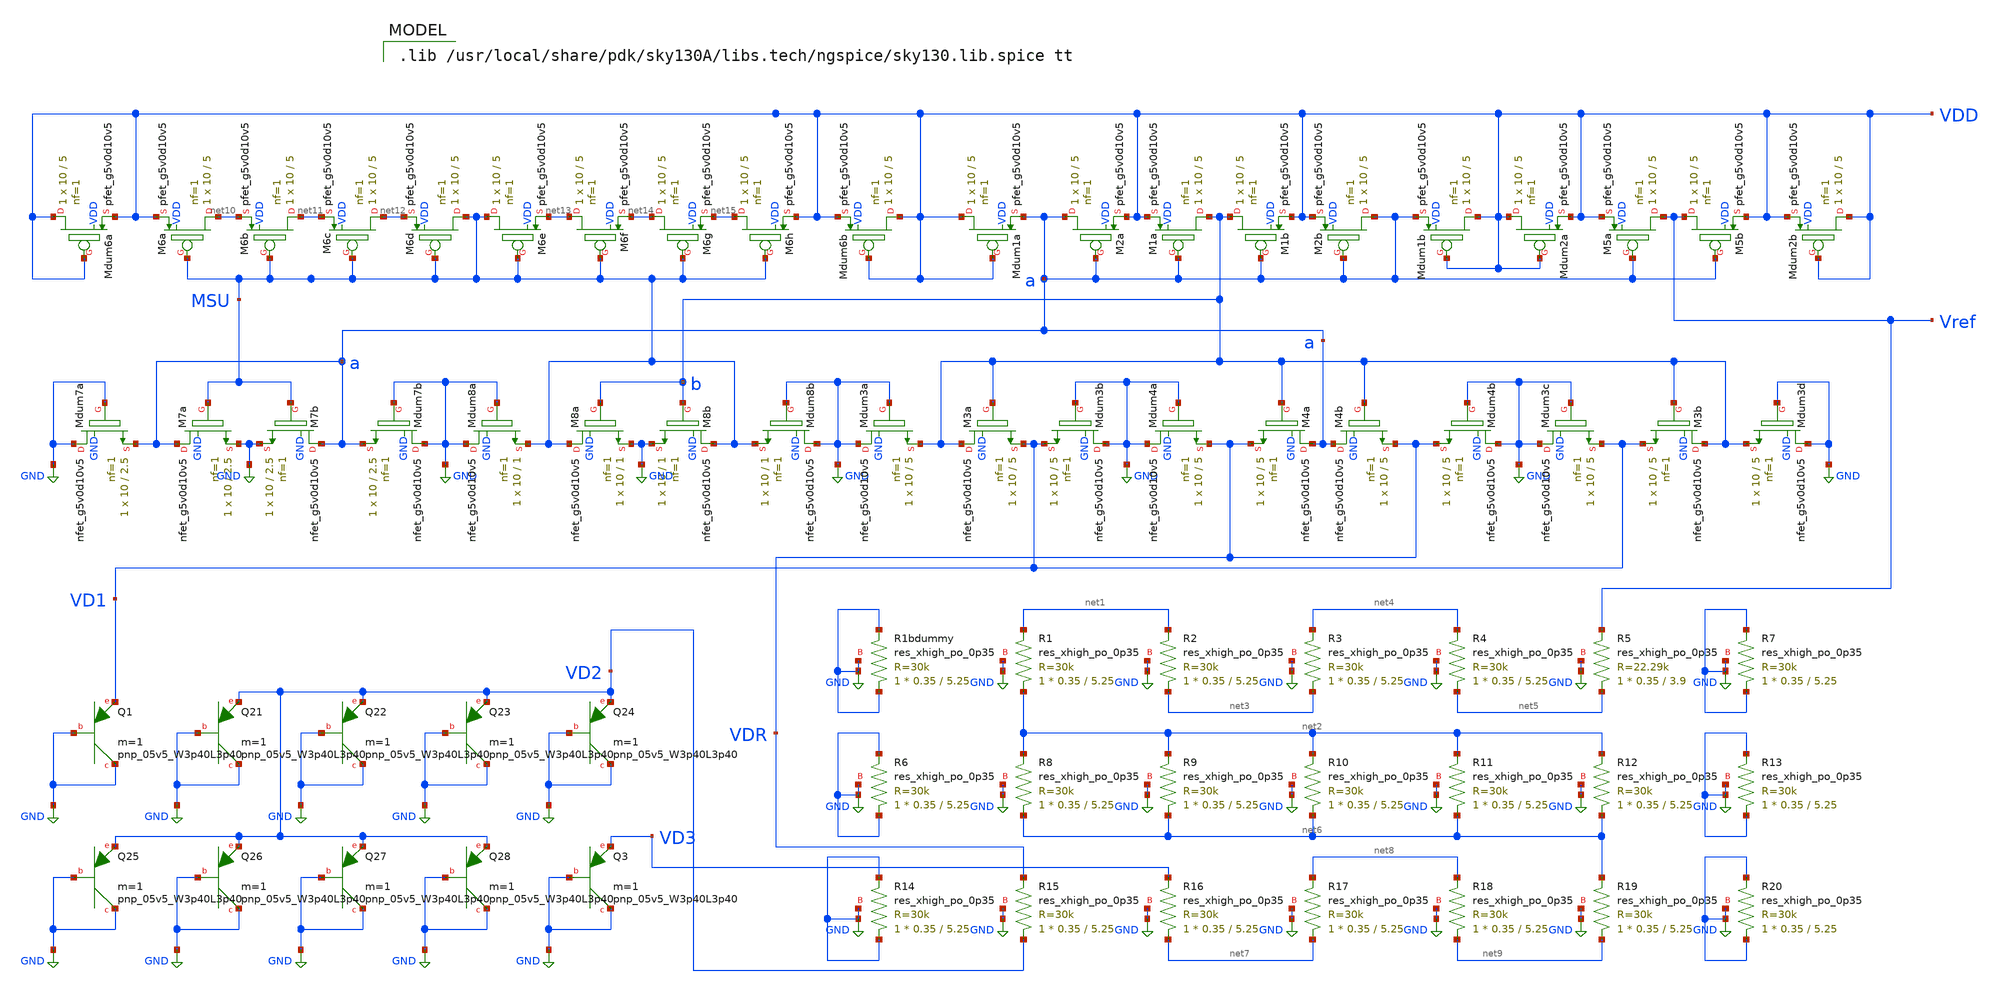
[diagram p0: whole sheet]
** sch_path: 2_BGR_nocas_30k_3p4pnp_floor.sch
**.subckt 2_BGR_nocas_30k_3p4pnp_floor
XM2a a a VDD VDD sky130_fd_pr__pfet_g5v0d10v5 L=5 W=10 nf=1 ad='int((nf+1)/2) * W/nf * 0.29' as='int((nf+2)/2) * W/nf * 0.29'
+ pd='2*int((nf+1)/2) * (W/nf + 0.29)' ps='2*int((nf+2)/2) * (W/nf + 0.29)' nrd='0.29 / W' nrs='0.29 / W'
+ sa=0 sb=0 sd=0 mult=1 m=1
XM1a b a VDD VDD sky130_fd_pr__pfet_g5v0d10v5 L=5 W=10 nf=1 ad='int((nf+1)/2) * W/nf * 0.29' as='int((nf+2)/2) * W/nf * 0.29'
+ pd='2*int((nf+1)/2) * (W/nf + 0.29)' ps='2*int((nf+2)/2) * (W/nf + 0.29)' nrd='0.29 / W' nrs='0.29 / W'
+ sa=0 sb=0 sd=0 mult=1 m=1
XM1b b a VDD VDD sky130_fd_pr__pfet_g5v0d10v5 L=5 W=10 nf=1 ad='int((nf+1)/2) * W/nf * 0.29' as='int((nf+2)/2) * W/nf * 0.29'
+ pd='2*int((nf+1)/2) * (W/nf + 0.29)' ps='2*int((nf+2)/2) * (W/nf + 0.29)' nrd='0.29 / W' nrs='0.29 / W'
+ sa=0 sb=0 sd=0 mult=1 m=1
XM2b a a VDD VDD sky130_fd_pr__pfet_g5v0d10v5 L=5 W=10 nf=1 ad='int((nf+1)/2) * W/nf * 0.29' as='int((nf+2)/2) * W/nf * 0.29'
+ pd='2*int((nf+1)/2) * (W/nf + 0.29)' ps='2*int((nf+2)/2) * (W/nf + 0.29)' nrd='0.29 / W' nrs='0.29 / W'
+ sa=0 sb=0 sd=0 mult=1 m=1
XM5a Vref a VDD VDD sky130_fd_pr__pfet_g5v0d10v5 L=5 W=10 nf=1 ad='int((nf+1)/2) * W/nf * 0.29' as='int((nf+2)/2) * W/nf * 0.29'
+ pd='2*int((nf+1)/2) * (W/nf + 0.29)' ps='2*int((nf+2)/2) * (W/nf + 0.29)' nrd='0.29 / W' nrs='0.29 / W'
+ sa=0 sb=0 sd=0 mult=1 m=1
XM5b Vref a VDD VDD sky130_fd_pr__pfet_g5v0d10v5 L=5 W=10 nf=1 ad='int((nf+1)/2) * W/nf * 0.29' as='int((nf+2)/2) * W/nf * 0.29'
+ pd='2*int((nf+1)/2) * (W/nf + 0.29)' ps='2*int((nf+2)/2) * (W/nf + 0.29)' nrd='0.29 / W' nrs='0.29 / W'
+ sa=0 sb=0 sd=0 mult=1 m=1
XR1bdummy GND GND GND sky130_fd_pr__res_xhigh_po_0p35 L=5.25 mult=1 m=1
XR1 net2 net1 GND sky130_fd_pr__res_xhigh_po_0p35 L=5.25 mult=1 m=1
XR2 net3 net1 GND sky130_fd_pr__res_xhigh_po_0p35 L=5.25 mult=1 m=1
XR3 net3 net4 GND sky130_fd_pr__res_xhigh_po_0p35 L=5.25 mult=1 m=1
XR4 net5 net4 GND sky130_fd_pr__res_xhigh_po_0p35 L=5.25 mult=1 m=1
XR5 net5 Vref GND sky130_fd_pr__res_xhigh_po_0p35 L=3.9 mult=1 m=1
XR8 net6 net2 GND sky130_fd_pr__res_xhigh_po_0p35 L=5.25 mult=1 m=1
XR9 net6 net2 GND sky130_fd_pr__res_xhigh_po_0p35 L=5.25 mult=1 m=1
XR10 net6 net2 GND sky130_fd_pr__res_xhigh_po_0p35 L=5.25 mult=1 m=1
XR11 net6 net2 GND sky130_fd_pr__res_xhigh_po_0p35 L=5.25 mult=1 m=1
XR12 net6 net2 GND sky130_fd_pr__res_xhigh_po_0p35 L=5.25 mult=1 m=1
XR14 GND GND GND sky130_fd_pr__res_xhigh_po_0p35 L=5.25 mult=1 m=1
XR15 VD2 VDR GND sky130_fd_pr__res_xhigh_po_0p35 L=5.25 mult=1 m=1
XR16 net7 VD3 GND sky130_fd_pr__res_xhigh_po_0p35 L=5.25 mult=1 m=1
XR17 net7 net8 GND sky130_fd_pr__res_xhigh_po_0p35 L=5.25 mult=1 m=1
XR18 net9 net8 GND sky130_fd_pr__res_xhigh_po_0p35 L=5.25 mult=1 m=1
XR19 net9 net6 GND sky130_fd_pr__res_xhigh_po_0p35 L=5.25 mult=1 m=1
XQ21 GND GND VD2 sky130_fd_pr__pnp_05v5_W3p40L3p40 m=1
XQ22 GND GND VD2 sky130_fd_pr__pnp_05v5_W3p40L3p40 m=1
XQ23 GND GND VD2 sky130_fd_pr__pnp_05v5_W3p40L3p40 m=1
XQ24 GND GND VD2 sky130_fd_pr__pnp_05v5_W3p40L3p40 m=1
XQ1 GND GND VD1 sky130_fd_pr__pnp_05v5_W3p40L3p40 m=1
XQ26 GND GND VD2 sky130_fd_pr__pnp_05v5_W3p40L3p40 m=1
XQ27 GND GND VD2 sky130_fd_pr__pnp_05v5_W3p40L3p40 m=1
XQ28 GND GND VD2 sky130_fd_pr__pnp_05v5_W3p40L3p40 m=1
XQ3 GND GND VD3 sky130_fd_pr__pnp_05v5_W3p40L3p40 m=1
XQ25 GND GND VD2 sky130_fd_pr__pnp_05v5_W3p40L3p40 m=1
XMdum1a VDD VDD a VDD sky130_fd_pr__pfet_g5v0d10v5 L=5 W=10 nf=1 ad='int((nf+1)/2) * W/nf * 0.29' as='int((nf+2)/2) * W/nf * 0.29'
+ pd='2*int((nf+1)/2) * (W/nf + 0.29)' ps='2*int((nf+2)/2) * (W/nf + 0.29)' nrd='0.29 / W' nrs='0.29 / W'
+ sa=0 sb=0 sd=0 mult=1 m=1
XMdum1b VDD VDD a VDD sky130_fd_pr__pfet_g5v0d10v5 L=5 W=10 nf=1 ad='int((nf+1)/2) * W/nf * 0.29' as='int((nf+2)/2) * W/nf * 0.29'
+ pd='2*int((nf+1)/2) * (W/nf + 0.29)' ps='2*int((nf+2)/2) * (W/nf + 0.29)' nrd='0.29 / W' nrs='0.29 / W'
+ sa=0 sb=0 sd=0 mult=1 m=1
XMdum2a VDD VDD VDD VDD sky130_fd_pr__pfet_g5v0d10v5 L=5 W=10 nf=1 ad='int((nf+1)/2) * W/nf * 0.29' as='int((nf+2)/2) * W/nf * 0.29'
+ pd='2*int((nf+1)/2) * (W/nf + 0.29)' ps='2*int((nf+2)/2) * (W/nf + 0.29)' nrd='0.29 / W' nrs='0.29 / W'
+ sa=0 sb=0 sd=0 mult=1 m=1
XMdum2b VDD VDD VDD VDD sky130_fd_pr__pfet_g5v0d10v5 L=5 W=10 nf=1 ad='int((nf+1)/2) * W/nf * 0.29' as='int((nf+2)/2) * W/nf * 0.29'
+ pd='2*int((nf+1)/2) * (W/nf + 0.29)' ps='2*int((nf+2)/2) * (W/nf + 0.29)' nrd='0.29 / W' nrs='0.29 / W'
+ sa=0 sb=0 sd=0 mult=1 m=1
XM6a net10 MSU VDD VDD sky130_fd_pr__pfet_g5v0d10v5 L=5 W=10 nf=1 ad='int((nf+1)/2) * W/nf * 0.29' as='int((nf+2)/2) * W/nf * 0.29'
+ pd='2*int((nf+1)/2) * (W/nf + 0.29)' ps='2*int((nf+2)/2) * (W/nf + 0.29)' nrd='0.29 / W' nrs='0.29 / W'
+ sa=0 sb=0 sd=0 mult=1 m=1
XM6b net11 MSU net10 VDD sky130_fd_pr__pfet_g5v0d10v5 L=5 W=10 nf=1 ad='int((nf+1)/2) * W/nf * 0.29'
+ as='int((nf+2)/2) * W/nf * 0.29' pd='2*int((nf+1)/2) * (W/nf + 0.29)' ps='2*int((nf+2)/2) * (W/nf + 0.29)'
+ nrd='0.29 / W' nrs='0.29 / W' sa=0 sb=0 sd=0 mult=1 m=1
XM6c net12 MSU net11 VDD sky130_fd_pr__pfet_g5v0d10v5 L=5 W=10 nf=1 ad='int((nf+1)/2) * W/nf * 0.29'
+ as='int((nf+2)/2) * W/nf * 0.29' pd='2*int((nf+1)/2) * (W/nf + 0.29)' ps='2*int((nf+2)/2) * (W/nf + 0.29)'
+ nrd='0.29 / W' nrs='0.29 / W' sa=0 sb=0 sd=0 mult=1 m=1
XM6d MSU MSU net12 VDD sky130_fd_pr__pfet_g5v0d10v5 L=5 W=10 nf=1 ad='int((nf+1)/2) * W/nf * 0.29' as='int((nf+2)/2) * W/nf * 0.29'
+ pd='2*int((nf+1)/2) * (W/nf + 0.29)' ps='2*int((nf+2)/2) * (W/nf + 0.29)' nrd='0.29 / W' nrs='0.29 / W'
+ sa=0 sb=0 sd=0 mult=1 m=1
XM6e MSU MSU net13 VDD sky130_fd_pr__pfet_g5v0d10v5 L=5 W=10 nf=1 ad='int((nf+1)/2) * W/nf * 0.29' as='int((nf+2)/2) * W/nf * 0.29'
+ pd='2*int((nf+1)/2) * (W/nf + 0.29)' ps='2*int((nf+2)/2) * (W/nf + 0.29)' nrd='0.29 / W' nrs='0.29 / W'
+ sa=0 sb=0 sd=0 mult=1 m=1
XM6f net13 MSU net14 VDD sky130_fd_pr__pfet_g5v0d10v5 L=5 W=10 nf=1 ad='int((nf+1)/2) * W/nf * 0.29'
+ as='int((nf+2)/2) * W/nf * 0.29' pd='2*int((nf+1)/2) * (W/nf + 0.29)' ps='2*int((nf+2)/2) * (W/nf + 0.29)'
+ nrd='0.29 / W' nrs='0.29 / W' sa=0 sb=0 sd=0 mult=1 m=1
XM6g net14 MSU net15 VDD sky130_fd_pr__pfet_g5v0d10v5 L=5 W=10 nf=1 ad='int((nf+1)/2) * W/nf * 0.29'
+ as='int((nf+2)/2) * W/nf * 0.29' pd='2*int((nf+1)/2) * (W/nf + 0.29)' ps='2*int((nf+2)/2) * (W/nf + 0.29)'
+ nrd='0.29 / W' nrs='0.29 / W' sa=0 sb=0 sd=0 mult=1 m=1
XM6h net15 MSU VDD VDD sky130_fd_pr__pfet_g5v0d10v5 L=5 W=10 nf=1 ad='int((nf+1)/2) * W/nf * 0.29' as='int((nf+2)/2) * W/nf * 0.29'
+ pd='2*int((nf+1)/2) * (W/nf + 0.29)' ps='2*int((nf+2)/2) * (W/nf + 0.29)' nrd='0.29 / W' nrs='0.29 / W'
+ sa=0 sb=0 sd=0 mult=1 m=1
XMdum6b VDD VDD VDD VDD sky130_fd_pr__pfet_g5v0d10v5 L=5 W=10 nf=1 ad='int((nf+1)/2) * W/nf * 0.29' as='int((nf+2)/2) * W/nf * 0.29'
+ pd='2*int((nf+1)/2) * (W/nf + 0.29)' ps='2*int((nf+2)/2) * (W/nf + 0.29)' nrd='0.29 / W' nrs='0.29 / W'
+ sa=0 sb=0 sd=0 mult=1 m=1
XMdum6a VDD VDD VDD VDD sky130_fd_pr__pfet_g5v0d10v5 L=5 W=10 nf=1 ad='int((nf+1)/2) * W/nf * 0.29' as='int((nf+2)/2) * W/nf * 0.29'
+ pd='2*int((nf+1)/2) * (W/nf + 0.29)' ps='2*int((nf+2)/2) * (W/nf + 0.29)' nrd='0.29 / W' nrs='0.29 / W'
+ sa=0 sb=0 sd=0 mult=1 m=1
XM7a a MSU GND GND sky130_fd_pr__nfet_g5v0d10v5 L=2.5 W=10 nf=1 ad='int((nf+1)/2) * W/nf * 0.29' as='int((nf+2)/2) * W/nf * 0.29'
+ pd='2*int((nf+1)/2) * (W/nf + 0.29)' ps='2*int((nf+2)/2) * (W/nf + 0.29)' nrd='0.29 / W' nrs='0.29 / W'
+ sa=0 sb=0 sd=0 mult=1 m=1
XM7b a MSU GND GND sky130_fd_pr__nfet_g5v0d10v5 L=2.5 W=10 nf=1 ad='int((nf+1)/2) * W/nf * 0.29' as='int((nf+2)/2) * W/nf * 0.29'
+ pd='2*int((nf+1)/2) * (W/nf + 0.29)' ps='2*int((nf+2)/2) * (W/nf + 0.29)' nrd='0.29 / W' nrs='0.29 / W'
+ sa=0 sb=0 sd=0 mult=1 m=1
XMdum7a GND GND a GND sky130_fd_pr__nfet_g5v0d10v5 L=2.5 W=10 nf=1 ad='int((nf+1)/2) * W/nf * 0.29' as='int((nf+2)/2) * W/nf * 0.29'
+ pd='2*int((nf+1)/2) * (W/nf + 0.29)' ps='2*int((nf+2)/2) * (W/nf + 0.29)' nrd='0.29 / W' nrs='0.29 / W'
+ sa=0 sb=0 sd=0 mult=1 m=1
XMdum7b GND GND a GND sky130_fd_pr__nfet_g5v0d10v5 L=2.5 W=10 nf=1 ad='int((nf+1)/2) * W/nf * 0.29' as='int((nf+2)/2) * W/nf * 0.29'
+ pd='2*int((nf+1)/2) * (W/nf + 0.29)' ps='2*int((nf+2)/2) * (W/nf + 0.29)' nrd='0.29 / W' nrs='0.29 / W'
+ sa=0 sb=0 sd=0 mult=1 m=1
XMdum8a GND GND MSU GND sky130_fd_pr__nfet_g5v0d10v5 L=1 W=10 nf=1 ad='int((nf+1)/2) * W/nf * 0.29' as='int((nf+2)/2) * W/nf * 0.29'
+ pd='2*int((nf+1)/2) * (W/nf + 0.29)' ps='2*int((nf+2)/2) * (W/nf + 0.29)' nrd='0.29 / W' nrs='0.29 / W'
+ sa=0 sb=0 sd=0 mult=1 m=1
XM8a MSU b GND GND sky130_fd_pr__nfet_g5v0d10v5 L=1 W=10 nf=1 ad='int((nf+1)/2) * W/nf * 0.29' as='int((nf+2)/2) * W/nf * 0.29'
+ pd='2*int((nf+1)/2) * (W/nf + 0.29)' ps='2*int((nf+2)/2) * (W/nf + 0.29)' nrd='0.29 / W' nrs='0.29 / W'
+ sa=0 sb=0 sd=0 mult=1 m=1
XM8b MSU b GND GND sky130_fd_pr__nfet_g5v0d10v5 L=1 W=10 nf=1 ad='int((nf+1)/2) * W/nf * 0.29' as='int((nf+2)/2) * W/nf * 0.29'
+ pd='2*int((nf+1)/2) * (W/nf + 0.29)' ps='2*int((nf+2)/2) * (W/nf + 0.29)' nrd='0.29 / W' nrs='0.29 / W'
+ sa=0 sb=0 sd=0 mult=1 m=1
XMdum8b GND GND MSU GND sky130_fd_pr__nfet_g5v0d10v5 L=1 W=10 nf=1 ad='int((nf+1)/2) * W/nf * 0.29' as='int((nf+2)/2) * W/nf * 0.29'
+ pd='2*int((nf+1)/2) * (W/nf + 0.29)' ps='2*int((nf+2)/2) * (W/nf + 0.29)' nrd='0.29 / W' nrs='0.29 / W'
+ sa=0 sb=0 sd=0 mult=1 m=1
XMdum3a GND GND b GND sky130_fd_pr__nfet_g5v0d10v5 L=5 W=10 nf=1 ad='int((nf+1)/2) * W/nf * 0.29' as='int((nf+2)/2) * W/nf * 0.29'
+ pd='2*int((nf+1)/2) * (W/nf + 0.29)' ps='2*int((nf+2)/2) * (W/nf + 0.29)' nrd='0.29 / W' nrs='0.29 / W'
+ sa=0 sb=0 sd=0 mult=1 m=1
XM3a b b VD1 GND sky130_fd_pr__nfet_g5v0d10v5 L=5 W=10 nf=1 ad='int((nf+1)/2) * W/nf * 0.29' as='int((nf+2)/2) * W/nf * 0.29'
+ pd='2*int((nf+1)/2) * (W/nf + 0.29)' ps='2*int((nf+2)/2) * (W/nf + 0.29)' nrd='0.29 / W' nrs='0.29 / W'
+ sa=0 sb=0 sd=0 mult=1 m=1
XMdum3b GND GND VD1 GND sky130_fd_pr__nfet_g5v0d10v5 L=5 W=10 nf=1 ad='int((nf+1)/2) * W/nf * 0.29' as='int((nf+2)/2) * W/nf * 0.29'
+ pd='2*int((nf+1)/2) * (W/nf + 0.29)' ps='2*int((nf+2)/2) * (W/nf + 0.29)' nrd='0.29 / W' nrs='0.29 / W'
+ sa=0 sb=0 sd=0 mult=1 m=1
XMdum4a GND GND VDR GND sky130_fd_pr__nfet_g5v0d10v5 L=5 W=10 nf=1 ad='int((nf+1)/2) * W/nf * 0.29' as='int((nf+2)/2) * W/nf * 0.29'
+ pd='2*int((nf+1)/2) * (W/nf + 0.29)' ps='2*int((nf+2)/2) * (W/nf + 0.29)' nrd='0.29 / W' nrs='0.29 / W'
+ sa=0 sb=0 sd=0 mult=1 m=1
XM4a a b VDR GND sky130_fd_pr__nfet_g5v0d10v5 L=5 W=10 nf=1 ad='int((nf+1)/2) * W/nf * 0.29' as='int((nf+2)/2) * W/nf * 0.29'
+ pd='2*int((nf+1)/2) * (W/nf + 0.29)' ps='2*int((nf+2)/2) * (W/nf + 0.29)' nrd='0.29 / W' nrs='0.29 / W'
+ sa=0 sb=0 sd=0 mult=1 m=1
XM4b a b VDR GND sky130_fd_pr__nfet_g5v0d10v5 L=5 W=10 nf=1 ad='int((nf+1)/2) * W/nf * 0.29' as='int((nf+2)/2) * W/nf * 0.29'
+ pd='2*int((nf+1)/2) * (W/nf + 0.29)' ps='2*int((nf+2)/2) * (W/nf + 0.29)' nrd='0.29 / W' nrs='0.29 / W'
+ sa=0 sb=0 sd=0 mult=1 m=1
XMdum4b GND GND VDR GND sky130_fd_pr__nfet_g5v0d10v5 L=5 W=10 nf=1 ad='int((nf+1)/2) * W/nf * 0.29' as='int((nf+2)/2) * W/nf * 0.29'
+ pd='2*int((nf+1)/2) * (W/nf + 0.29)' ps='2*int((nf+2)/2) * (W/nf + 0.29)' nrd='0.29 / W' nrs='0.29 / W'
+ sa=0 sb=0 sd=0 mult=1 m=1
XMdum3c GND GND VD1 GND sky130_fd_pr__nfet_g5v0d10v5 L=5 W=10 nf=1 ad='int((nf+1)/2) * W/nf * 0.29' as='int((nf+2)/2) * W/nf * 0.29'
+ pd='2*int((nf+1)/2) * (W/nf + 0.29)' ps='2*int((nf+2)/2) * (W/nf + 0.29)' nrd='0.29 / W' nrs='0.29 / W'
+ sa=0 sb=0 sd=0 mult=1 m=1
XM3b b b VD1 GND sky130_fd_pr__nfet_g5v0d10v5 L=5 W=10 nf=1 ad='int((nf+1)/2) * W/nf * 0.29' as='int((nf+2)/2) * W/nf * 0.29'
+ pd='2*int((nf+1)/2) * (W/nf + 0.29)' ps='2*int((nf+2)/2) * (W/nf + 0.29)' nrd='0.29 / W' nrs='0.29 / W'
+ sa=0 sb=0 sd=0 mult=1 m=1
XMdum3d GND GND b GND sky130_fd_pr__nfet_g5v0d10v5 L=5 W=10 nf=1 ad='int((nf+1)/2) * W/nf * 0.29' as='int((nf+2)/2) * W/nf * 0.29'
+ pd='2*int((nf+1)/2) * (W/nf + 0.29)' ps='2*int((nf+2)/2) * (W/nf + 0.29)' nrd='0.29 / W' nrs='0.29 / W'
+ sa=0 sb=0 sd=0 mult=1 m=1
XR6 GND GND GND sky130_fd_pr__res_xhigh_po_0p35 L=5.25 mult=1 m=1
XR7 GND GND GND sky130_fd_pr__res_xhigh_po_0p35 L=5.25 mult=1 m=1
XR13 GND GND GND sky130_fd_pr__res_xhigh_po_0p35 L=5.25 mult=1 m=1
XR20 GND GND GND sky130_fd_pr__res_xhigh_po_0p35 L=5.25 mult=1 m=1
**** begin user architecture code

.save all
Vdd Vdd 0 DC 0 AC 0
*** Plot color settings***
.control
set color0=white  color1=black color2=blue color3=red
set color4=magenta  color5=cyan  xbrushwidth=3
.endc
*** Temp variation ***
.control
alter Vdd DC=3.3
dc temp -40 125 0.1
plot V1#branch V2#branch V3#branch
plot VD3
plot V(Vref,VD3)
plot Vref
.endc
*************************
*** Supply variation ***
.control
dc Vdd 2 5.5 1m
plot Vref Vdd
.endc
************************
*** PSRR analysis ***
.control
alter Vdd DC=3.3
alter Vdd AC=1
ac dec 10 1 10G
plot db(Vref)
.endc
*************************
*** Transient analysis ***
.control
alter @Vdd[pwl]=[ 0 0 100u 0 200u 3.3 500u 3.3 ]
tran 100u 500u
plot Vdd Vref
.endc
************************
.end


.lib /usr/local/share/pdk/sky130A/libs.tech/ngspice/sky130.lib.spice tt

**** end user architecture code
**.ends
.GLOBAL GND
.end
